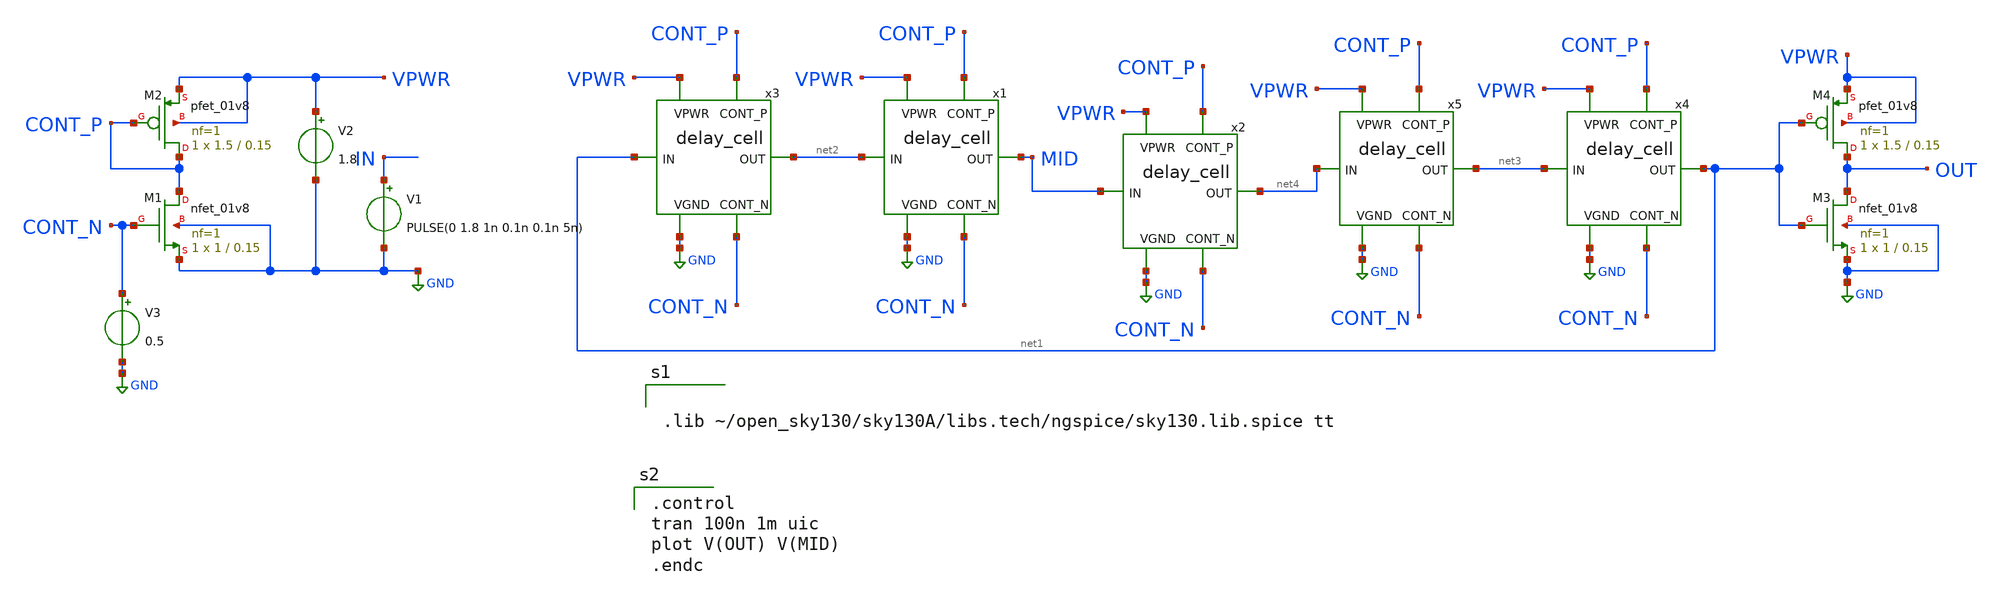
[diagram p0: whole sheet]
** sch_path: xschem/ring_osc/delay_cell_tb.sch
**.subckt delay_cell_tb
x1 VPWR CONT_P net2 MID CONT_N GND delay_cell
V1 IN GND PULSE(0 1.8 1n 0.1n 0.1n 5n)
V2 VPWR GND 1.8
XM1 CONT_P CONT_N GND GND sky130_fd_pr__nfet_01v8 L=0.15 W=1 nf=1 ad='int((nf+1)/2) * W/nf * 0.29' as='int((nf+2)/2) * W/nf * 0.29'
+ pd='2*int((nf+1)/2) * (W/nf + 0.29)' ps='2*int((nf+2)/2) * (W/nf + 0.29)' nrd='0.29 / W' nrs='0.29 / W'
+ sa=0 sb=0 sd=0 mult=1 m=1
XM2 CONT_P CONT_P VPWR VPWR sky130_fd_pr__pfet_01v8 L=0.15 W=1.5 nf=1 ad='int((nf+1)/2) * W/nf * 0.29'
+ as='int((nf+2)/2) * W/nf * 0.29' pd='2*int((nf+1)/2) * (W/nf + 0.29)' ps='2*int((nf+2)/2) * (W/nf + 0.29)'
+ nrd='0.29 / W' nrs='0.29 / W' sa=0 sb=0 sd=0 mult=1 m=1
V3 CONT_N GND 0.5
x2 VPWR CONT_P MID net4 CONT_N GND delay_cell
x3 VPWR CONT_P net1 net2 CONT_N GND delay_cell
x4 VPWR CONT_P net3 net1 CONT_N GND delay_cell
x5 VPWR CONT_P net4 net3 CONT_N GND delay_cell
XM3 OUT net1 GND GND sky130_fd_pr__nfet_01v8 L=0.15 W=1 nf=1 ad='int((nf+1)/2) * W/nf * 0.29' as='int((nf+2)/2) * W/nf * 0.29'
+ pd='2*int((nf+1)/2) * (W/nf + 0.29)' ps='2*int((nf+2)/2) * (W/nf + 0.29)' nrd='0.29 / W' nrs='0.29 / W'
+ sa=0 sb=0 sd=0 mult=1 m=1
XM4 OUT net1 VPWR VPWR sky130_fd_pr__pfet_01v8 L=0.15 W=1.5 nf=1 ad='int((nf+1)/2) * W/nf * 0.29' as='int((nf+2)/2) * W/nf * 0.29'
+ pd='2*int((nf+1)/2) * (W/nf + 0.29)' ps='2*int((nf+2)/2) * (W/nf + 0.29)' nrd='0.29 / W' nrs='0.29 / W'
+ sa=0 sb=0 sd=0 mult=1 m=1
**** begin user architecture code


.lib ~/open_sky130/sky130A/libs.tech/ngspice/sky130.lib.spice tt


.control
tran 100n 1m uic
plot V(OUT) V(MID)
.endc

**** end user architecture code
**.ends

* expanding   symbol:  delay_cell.sym # of pins=6
** sym_path: xschem/ring_osc/delay_cell.sym
** sch_path: xschem/ring_osc/delay_cell.sch
.subckt delay_cell VPWR CONT_P IN OUT CONT_N VGND
*.ipin VPWR
*.ipin VGND
*.ipin IN
*.ipin CONT_N
*.ipin CONT_P
*.opin OUT
XM1 OUT IN net1 VGND sky130_fd_pr__nfet_01v8 L=0.15 W=1 nf=1 ad='int((nf+1)/2) * W/nf * 0.29' as='int((nf+2)/2) * W/nf * 0.29'
+ pd='2*int((nf+1)/2) * (W/nf + 0.29)' ps='2*int((nf+2)/2) * (W/nf + 0.29)' nrd='0.29 / W' nrs='0.29 / W'
+ sa=0 sb=0 sd=0 mult=1 m=1
XM2 net1 CONT_N VGND VGND sky130_fd_pr__nfet_01v8 L=0.15 W=1 nf=1 ad='int((nf+1)/2) * W/nf * 0.29' as='int((nf+2)/2) * W/nf * 0.29'
+ pd='2*int((nf+1)/2) * (W/nf + 0.29)' ps='2*int((nf+2)/2) * (W/nf + 0.29)' nrd='0.29 / W' nrs='0.29 / W'
+ sa=0 sb=0 sd=0 mult=1 m=1
XM3 OUT IN net2 VPWR sky130_fd_pr__pfet_01v8 L=0.15 W=1.5 nf=1 ad='int((nf+1)/2) * W/nf * 0.29' as='int((nf+2)/2) * W/nf * 0.29'
+ pd='2*int((nf+1)/2) * (W/nf + 0.29)' ps='2*int((nf+2)/2) * (W/nf + 0.29)' nrd='0.29 / W' nrs='0.29 / W'
+ sa=0 sb=0 sd=0 mult=1 m=1
XM4 net2 CONT_P VPWR VPWR sky130_fd_pr__pfet_01v8 L=0.15 W=1.5 nf=1 ad='int((nf+1)/2) * W/nf * 0.29'
+ as='int((nf+2)/2) * W/nf * 0.29' pd='2*int((nf+1)/2) * (W/nf + 0.29)' ps='2*int((nf+2)/2) * (W/nf + 0.29)'
+ nrd='0.29 / W' nrs='0.29 / W' sa=0 sb=0 sd=0 mult=1 m=1
.ends

.GLOBAL GND
.end
